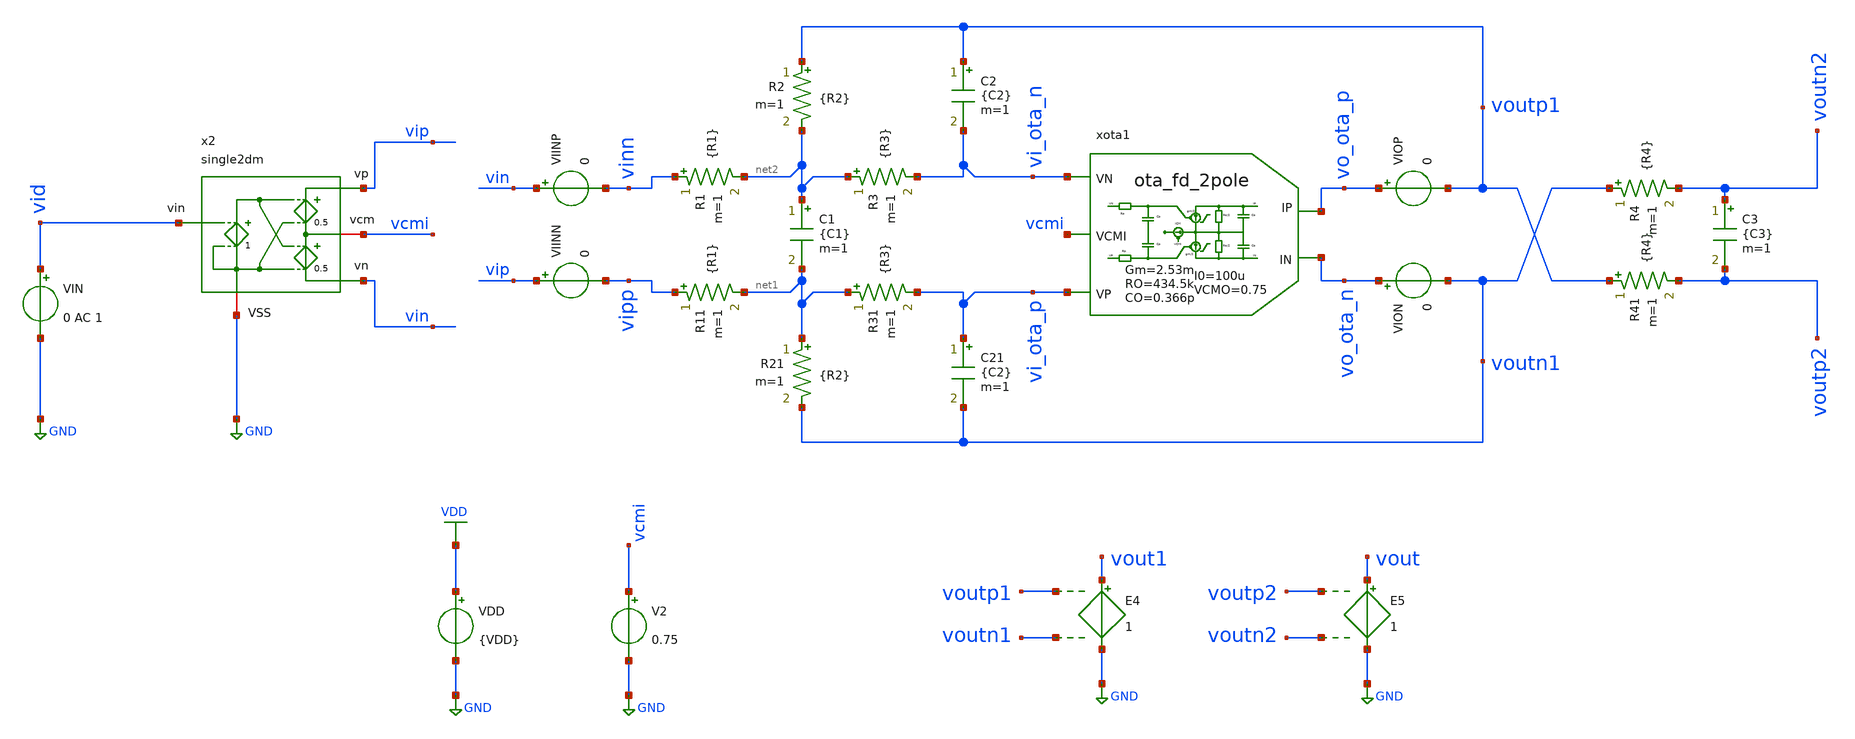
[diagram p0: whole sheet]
** sch_path: macros/filter_cmos5l/verification/chipify/tb/filter_cl_ideal.sch
**.subckt filter_cl_ideal
VIN vid GND 0 AC 1
E4 vout1 GND voutp1 voutn1 1
VIINP vin vinn 0
VIINN vip vipp 0
R1 vinn net2 {R1} m=1
R2 voutp1 net2 {R2} m=1
R3 net2 vi_ota_n {R3} m=1
C1 net2 net1 {C1} m=1
C3 voutn2 voutp2 {C3} m=1
R11 vipp net1 {R1} m=1
R21 net1 voutn1 {R2} m=1
R31 net1 vi_ota_p {R3} m=1
C21 vi_ota_p voutn1 {C2} m=1
R4 voutn1 voutn2 {R4} m=1
R41 voutp1 voutp2 {R4} m=1
C2 voutp1 vi_ota_n {C2} m=1
E5 vout GND voutp2 voutn2 1
VIOP vo_ota_p voutp1 0
VION vo_ota_n voutn1 0
VDD VDD GND {VDD}
x2 vip vid vcmi GND vin single2dm
V2 vcmi GND 0.75
xota1 vi_ota_n vo_ota_p vo_ota_n vi_ota_p vcmi ota_fd_2pole GM=2.53m RO=434.5k CO=0.366p RP=0
+ CP=0.1p VCMO=0.75 I0=100u
**** begin user architecture code


.include /foss/designs/kvosid_336004_ss26/macros/filter_cmos5l/scripts/sizing/filterPassives.spice
.param VDD = {{ VDD }}
.options savecurrents
.options method=gear reltol=.005
.options sparse
.control

let f_min = 10
let f_max = 100Meg
let f_stop = 9Meg
let f_nmin = 100
let f_nmax = 5Meg

let n_bits = 8
let Adc = 10
let v_fs = 1.0
let v_lsb = v_fs/2^n_bits
let v_qn = v_lsb/sqrt(12)
let err_gain_spec = v_lsb/v_fs
let vo_n_max = 113e-6

let v_step_o = v_fs
let v_step_i = v_step_o/Adc

let t_rf = 0.1u
let t_step = 50u
let t_delay = 0
let t_per = 2*t_step

let tstep = 0.1*t_rf
let tstop = 2*t_per
let tstart = t_delay

*op
ac dec 100 $&const.f_min $&const.f_max
*tran $&tstep $&tstop $&tstart

quit
.endc

**** end user architecture code
**.ends

* expanding   symbol:  single2dm.sym # of pins=5
** sym_path: single2dm.sym
** sch_path: single2dm.sch
.subckt single2dm vp vin vcm VSS vn
*.ipin vin
*.opin vn
*.iopin vcm
*.opin vp
*.iopin VSS
E3 vcm vn net1 VSS 0.5
E2 vp vcm net1 VSS 0.5
E1 net1 VSS vin VSS 1
.ends


* expanding   symbol:  ota_fd_2pole.sym # of pins=5
** sym_path: ota_fd_2pole.sym
** sch_path: ota_fd_2pole.sch
.subckt ota_fd_2pole VN IP IN VP VCMI  GM=1u RO=100Meg CO=1p RP=0 CP=0.1p VCMO=0 I0=1u
*.ipin VP
*.ipin VN
*.opin IP
*.opin IN
*.ipin VCMI
R3 IP net1 {RO/2} m=1
R4 IN net1 {RO/2} m=1
C3 IP net1 {CO} m=1
R5 VN ip1 {RP} m=1
C4 ip1 VCMI {CP} m=1
C6 in1 VCMI {CP} m=1
C8 IN net1 {CO} m=1
R7 VP in1 {RP} m=1
B2 IP net1 I = {I0*tanh(GM/2*V(ip1,in1)/I0)}
B1 net1 IN I = {I0*tanh(GM/2*V(ip1,in1)/I0)}
B5 net1 GND I = {VCMO-(V(IP)+V(IN))/2}
.ends

.GLOBAL GND
.GLOBAL VDD
.end
